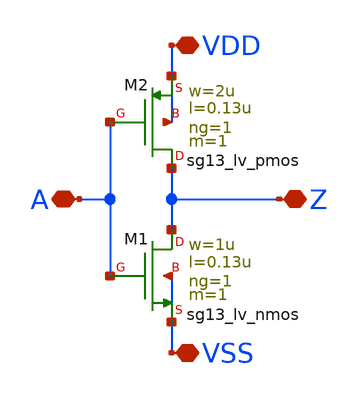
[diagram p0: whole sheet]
** sch_path: analog/core/inv_1x_gen.sch
**.subckt inv_1x_gen VDD VSS A Z
*.iopin VDD
*.iopin VSS
*.iopin A
*.iopin Z
XM1 Z A VSS VSS sg13_lv_nmos w=1u l=0.13u ng=1 m=1 mm_ok=1
XM2 Z A VDD VDD sg13_lv_pmos w=2u l=0.13u ng=1 m=1 mm_ok=1
**.ends
.end
